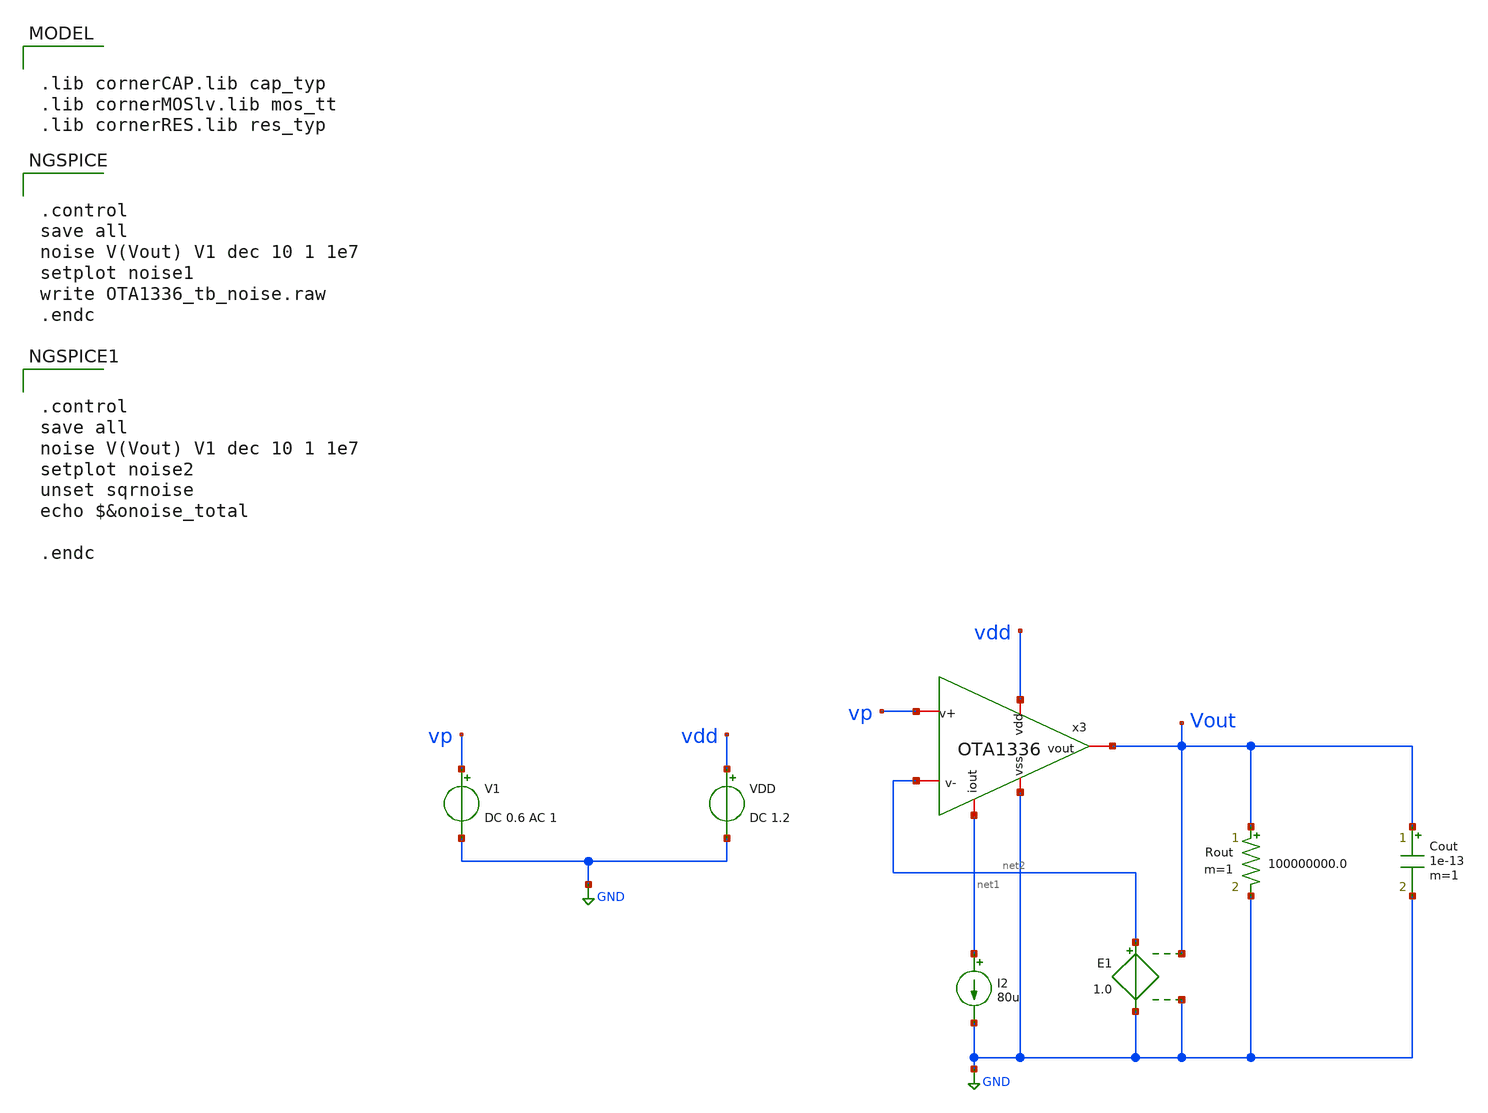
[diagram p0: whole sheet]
** sch_path: tests/data/OTA1336/testbenches/noise/xschem/OTA1336_noise_tb.sch
**.subckt OTA1336_noise_tb
V1 vp GND DC 0.6 AC 1
VDD vdd GND DC 1.2
I2 net1 GND 80u
x3 vdd net1 Vout net2 vp GND OTA1336
E1 net2 GND Vout GND 1.0
Rout Vout GND 100000000.0 m=1
Cout Vout GND 1e-13 m=1
**** begin user architecture code

.lib cornerCAP.lib cap_typ
.lib cornerMOSlv.lib mos_tt
.lib cornerRES.lib res_typ



.control
save all
noise V(Vout) V1 dec 10 1 1e7
setplot noise1
write OTA1336_tb_noise.raw
.endc




.control
save all
noise V(Vout) V1 dec 10 1 1e7
setplot noise2
unset sqrnoise
echo $&onoise_total

.endc


**** end user architecture code
**.ends
.GLOBAL GND
.end
